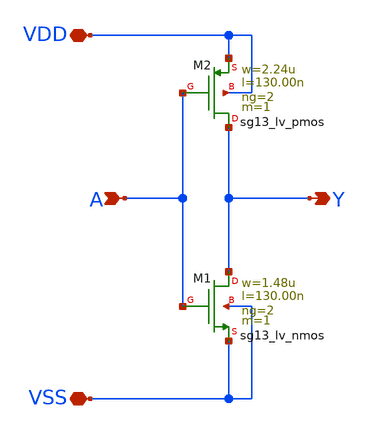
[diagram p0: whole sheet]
** sch_path: ihp-sg13g2/libs.tech/xschem/sg13g2_stdcells/sg13g2_inv_2.sch
**.subckt sg13g2_inv_2 Y A VDD VSS
*.opin Y
*.ipin A
*.iopin VDD
*.iopin VSS
XM1 Y A VSS VSS sg13_lv_nmos w=1.48u l=130.00n ng=2 m=1 mm_ok=1
XM2 Y A VDD VDD sg13_lv_pmos w=2.24u l=130.00n ng=2 m=1 mm_ok=1
**.ends
.end
